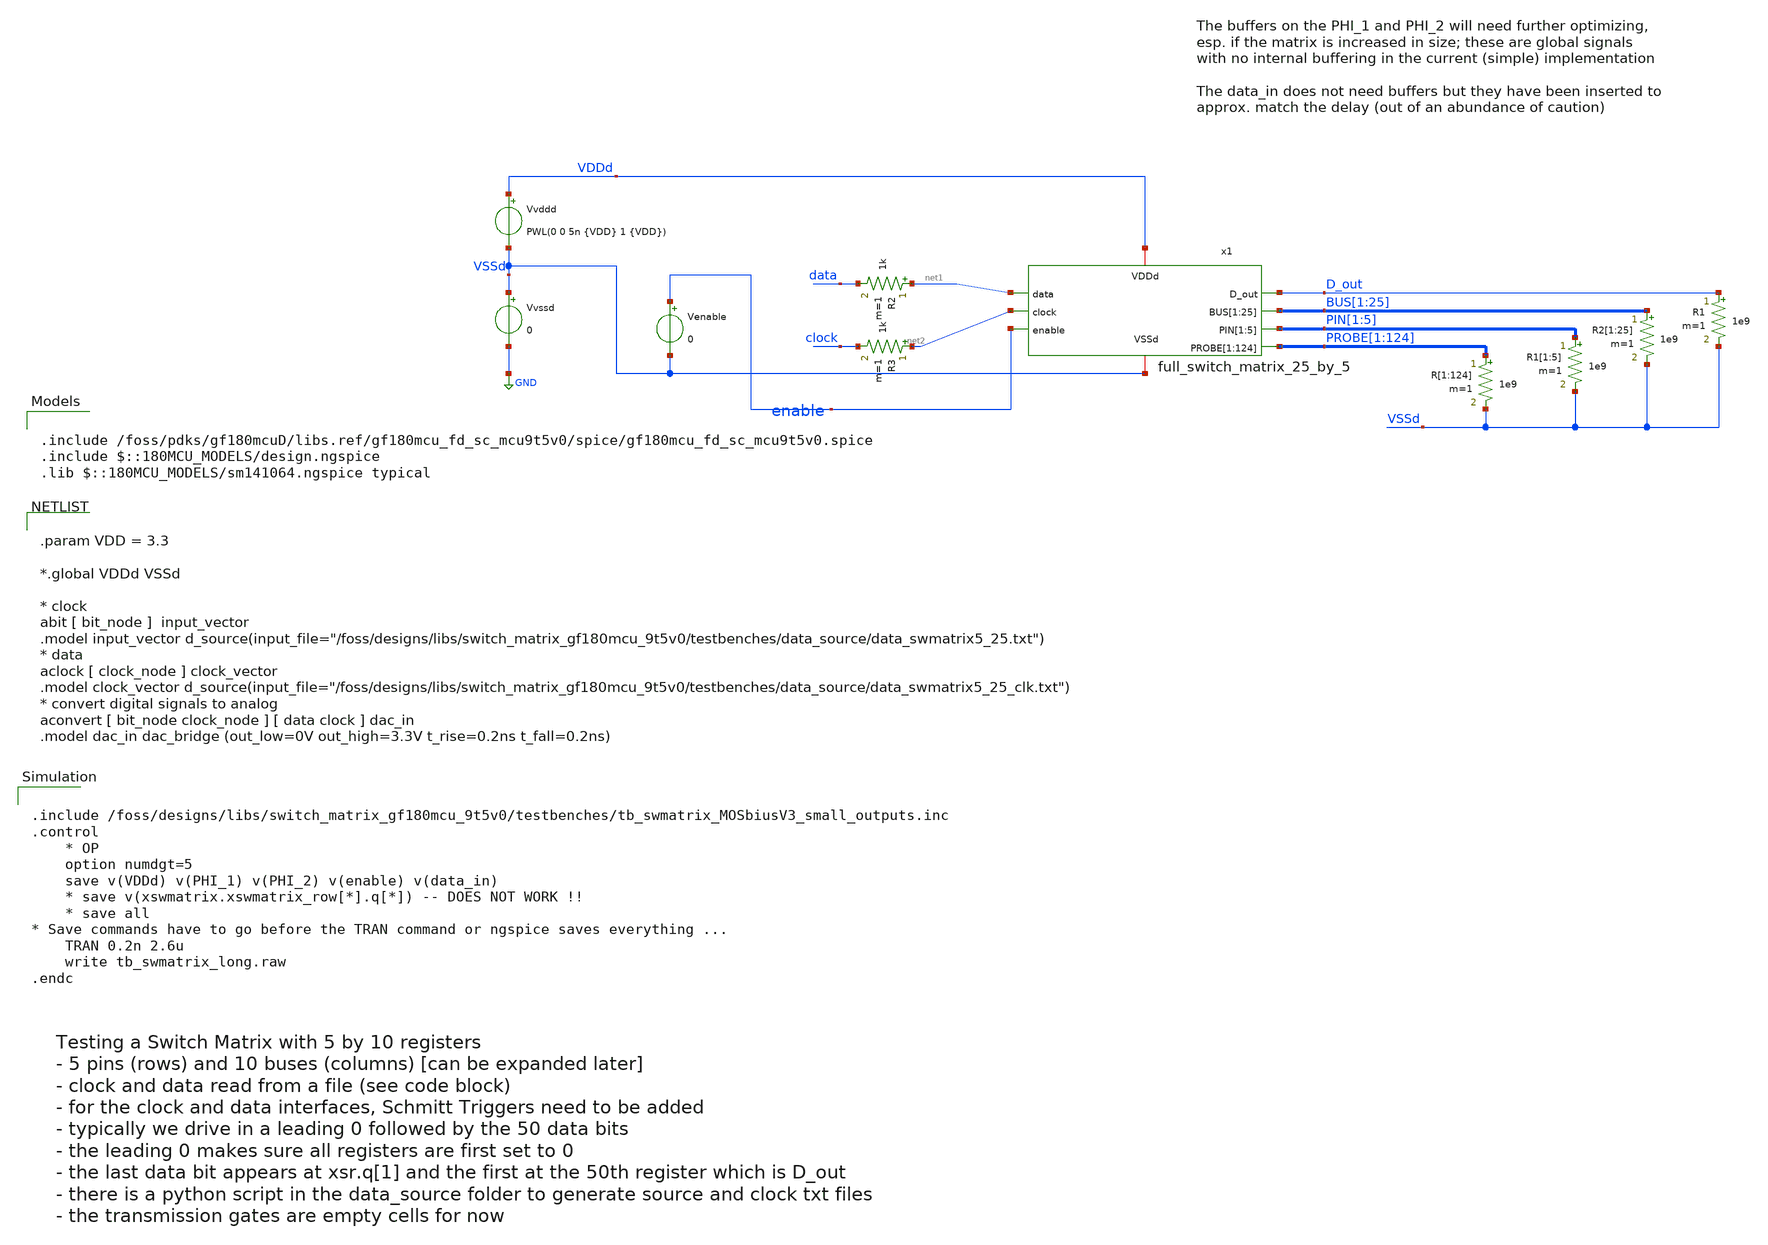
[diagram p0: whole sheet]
** sch_path: testbenches/tb_full_swmatrix_25_by_5.sch
**.subckt tb_full_swmatrix_25_by_5
Vvssd VSSd GND 0
Vvddd VDDd VSSd PWL(0 0 5n {VDD} 1 {VDD})
Venable enable VSSd 0
R2 net1 data 1k m=1
R3 net2 clock 1k m=1
x1 net1 D_out net2 BUS[1] BUS[2] BUS[3] BUS[4] BUS[5] BUS[6] BUS[7] BUS[8] BUS[9] BUS[10] BUS[11]
+ BUS[12] BUS[13] BUS[14] BUS[15] BUS[16] BUS[17] BUS[18] BUS[19] BUS[20] BUS[21] BUS[22] BUS[23] BUS[24]
+ BUS[25] PIN[1] PIN[2] PIN[3] PIN[4] PIN[5] enable VDDd VSSd PROBE[1] PROBE[2] PROBE[3] PROBE[4] PROBE[5]
+ PROBE[6] PROBE[7] PROBE[8] PROBE[9] PROBE[10] PROBE[11] PROBE[12] PROBE[13] PROBE[14] PROBE[15] PROBE[16]
+ PROBE[17] PROBE[18] PROBE[19] PROBE[20] PROBE[21] PROBE[22] PROBE[23] PROBE[24] PROBE[25] PROBE[26] PROBE[27]
+ PROBE[28] PROBE[29] PROBE[30] PROBE[31] PROBE[32] PROBE[33] PROBE[34] PROBE[35] PROBE[36] PROBE[37] PROBE[38]
+ PROBE[39] PROBE[40] PROBE[41] PROBE[42] PROBE[43] PROBE[44] PROBE[45] PROBE[46] PROBE[47] PROBE[48] PROBE[49]
+ PROBE[50] PROBE[51] PROBE[52] PROBE[53] PROBE[54] PROBE[55] PROBE[56] PROBE[57] PROBE[58] PROBE[59] PROBE[60]
+ PROBE[61] PROBE[62] PROBE[63] PROBE[64] PROBE[65] PROBE[66] PROBE[67] PROBE[68] PROBE[69] PROBE[70] PROBE[71]
+ PROBE[72] PROBE[73] PROBE[74] PROBE[75] PROBE[76] PROBE[77] PROBE[78] PROBE[79] PROBE[80] PROBE[81] PROBE[82]
+ PROBE[83] PROBE[84] PROBE[85] PROBE[86] PROBE[87] PROBE[88] PROBE[89] PROBE[90] PROBE[91] PROBE[92] PROBE[93]
+ PROBE[94] PROBE[95] PROBE[96] PROBE[97] PROBE[98] PROBE[99] PROBE[100] PROBE[101] PROBE[102] PROBE[103]
+ PROBE[104] PROBE[105] PROBE[106] PROBE[107] PROBE[108] PROBE[109] PROBE[110] PROBE[111] PROBE[112] PROBE[113]
+ PROBE[114] PROBE[115] PROBE[116] PROBE[117] PROBE[118] PROBE[119] PROBE[120] PROBE[121] PROBE[122] PROBE[123]
+ PROBE[124] full_switch_matrix_25_by_5
R[1] PROBE[1] VSSd 1e9 m=1
R[2] PROBE[2] VSSd 1e9 m=1
R[3] PROBE[3] VSSd 1e9 m=1
R[4] PROBE[4] VSSd 1e9 m=1
R[5] PROBE[5] VSSd 1e9 m=1
R[6] PROBE[6] VSSd 1e9 m=1
R[7] PROBE[7] VSSd 1e9 m=1
R[8] PROBE[8] VSSd 1e9 m=1
R[9] PROBE[9] VSSd 1e9 m=1
R[10] PROBE[10] VSSd 1e9 m=1
R[11] PROBE[11] VSSd 1e9 m=1
R[12] PROBE[12] VSSd 1e9 m=1
R[13] PROBE[13] VSSd 1e9 m=1
R[14] PROBE[14] VSSd 1e9 m=1
R[15] PROBE[15] VSSd 1e9 m=1
R[16] PROBE[16] VSSd 1e9 m=1
R[17] PROBE[17] VSSd 1e9 m=1
R[18] PROBE[18] VSSd 1e9 m=1
R[19] PROBE[19] VSSd 1e9 m=1
R[20] PROBE[20] VSSd 1e9 m=1
R[21] PROBE[21] VSSd 1e9 m=1
R[22] PROBE[22] VSSd 1e9 m=1
R[23] PROBE[23] VSSd 1e9 m=1
R[24] PROBE[24] VSSd 1e9 m=1
R[25] PROBE[25] VSSd 1e9 m=1
R[26] PROBE[26] VSSd 1e9 m=1
R[27] PROBE[27] VSSd 1e9 m=1
R[28] PROBE[28] VSSd 1e9 m=1
R[29] PROBE[29] VSSd 1e9 m=1
R[30] PROBE[30] VSSd 1e9 m=1
R[31] PROBE[31] VSSd 1e9 m=1
R[32] PROBE[32] VSSd 1e9 m=1
R[33] PROBE[33] VSSd 1e9 m=1
R[34] PROBE[34] VSSd 1e9 m=1
R[35] PROBE[35] VSSd 1e9 m=1
R[36] PROBE[36] VSSd 1e9 m=1
R[37] PROBE[37] VSSd 1e9 m=1
R[38] PROBE[38] VSSd 1e9 m=1
R[39] PROBE[39] VSSd 1e9 m=1
R[40] PROBE[40] VSSd 1e9 m=1
R[41] PROBE[41] VSSd 1e9 m=1
R[42] PROBE[42] VSSd 1e9 m=1
R[43] PROBE[43] VSSd 1e9 m=1
R[44] PROBE[44] VSSd 1e9 m=1
R[45] PROBE[45] VSSd 1e9 m=1
R[46] PROBE[46] VSSd 1e9 m=1
R[47] PROBE[47] VSSd 1e9 m=1
R[48] PROBE[48] VSSd 1e9 m=1
R[49] PROBE[49] VSSd 1e9 m=1
R[50] PROBE[50] VSSd 1e9 m=1
R[51] PROBE[51] VSSd 1e9 m=1
R[52] PROBE[52] VSSd 1e9 m=1
R[53] PROBE[53] VSSd 1e9 m=1
R[54] PROBE[54] VSSd 1e9 m=1
R[55] PROBE[55] VSSd 1e9 m=1
R[56] PROBE[56] VSSd 1e9 m=1
R[57] PROBE[57] VSSd 1e9 m=1
R[58] PROBE[58] VSSd 1e9 m=1
R[59] PROBE[59] VSSd 1e9 m=1
R[60] PROBE[60] VSSd 1e9 m=1
R[61] PROBE[61] VSSd 1e9 m=1
R[62] PROBE[62] VSSd 1e9 m=1
R[63] PROBE[63] VSSd 1e9 m=1
R[64] PROBE[64] VSSd 1e9 m=1
R[65] PROBE[65] VSSd 1e9 m=1
R[66] PROBE[66] VSSd 1e9 m=1
R[67] PROBE[67] VSSd 1e9 m=1
R[68] PROBE[68] VSSd 1e9 m=1
R[69] PROBE[69] VSSd 1e9 m=1
R[70] PROBE[70] VSSd 1e9 m=1
R[71] PROBE[71] VSSd 1e9 m=1
R[72] PROBE[72] VSSd 1e9 m=1
R[73] PROBE[73] VSSd 1e9 m=1
R[74] PROBE[74] VSSd 1e9 m=1
R[75] PROBE[75] VSSd 1e9 m=1
R[76] PROBE[76] VSSd 1e9 m=1
R[77] PROBE[77] VSSd 1e9 m=1
R[78] PROBE[78] VSSd 1e9 m=1
R[79] PROBE[79] VSSd 1e9 m=1
R[80] PROBE[80] VSSd 1e9 m=1
R[81] PROBE[81] VSSd 1e9 m=1
R[82] PROBE[82] VSSd 1e9 m=1
R[83] PROBE[83] VSSd 1e9 m=1
R[84] PROBE[84] VSSd 1e9 m=1
R[85] PROBE[85] VSSd 1e9 m=1
R[86] PROBE[86] VSSd 1e9 m=1
R[87] PROBE[87] VSSd 1e9 m=1
R[88] PROBE[88] VSSd 1e9 m=1
R[89] PROBE[89] VSSd 1e9 m=1
R[90] PROBE[90] VSSd 1e9 m=1
R[91] PROBE[91] VSSd 1e9 m=1
R[92] PROBE[92] VSSd 1e9 m=1
R[93] PROBE[93] VSSd 1e9 m=1
R[94] PROBE[94] VSSd 1e9 m=1
R[95] PROBE[95] VSSd 1e9 m=1
R[96] PROBE[96] VSSd 1e9 m=1
R[97] PROBE[97] VSSd 1e9 m=1
R[98] PROBE[98] VSSd 1e9 m=1
R[99] PROBE[99] VSSd 1e9 m=1
R[100] PROBE[100] VSSd 1e9 m=1
R[101] PROBE[101] VSSd 1e9 m=1
R[102] PROBE[102] VSSd 1e9 m=1
R[103] PROBE[103] VSSd 1e9 m=1
R[104] PROBE[104] VSSd 1e9 m=1
R[105] PROBE[105] VSSd 1e9 m=1
R[106] PROBE[106] VSSd 1e9 m=1
R[107] PROBE[107] VSSd 1e9 m=1
R[108] PROBE[108] VSSd 1e9 m=1
R[109] PROBE[109] VSSd 1e9 m=1
R[110] PROBE[110] VSSd 1e9 m=1
R[111] PROBE[111] VSSd 1e9 m=1
R[112] PROBE[112] VSSd 1e9 m=1
R[113] PROBE[113] VSSd 1e9 m=1
R[114] PROBE[114] VSSd 1e9 m=1
R[115] PROBE[115] VSSd 1e9 m=1
R[116] PROBE[116] VSSd 1e9 m=1
R[117] PROBE[117] VSSd 1e9 m=1
R[118] PROBE[118] VSSd 1e9 m=1
R[119] PROBE[119] VSSd 1e9 m=1
R[120] PROBE[120] VSSd 1e9 m=1
R[121] PROBE[121] VSSd 1e9 m=1
R[122] PROBE[122] VSSd 1e9 m=1
R[123] PROBE[123] VSSd 1e9 m=1
R[124] PROBE[124] VSSd 1e9 m=1
R1[1] PIN[1] VSSd 1e9 m=1
R1[2] PIN[2] VSSd 1e9 m=1
R1[3] PIN[3] VSSd 1e9 m=1
R1[4] PIN[4] VSSd 1e9 m=1
R1[5] PIN[5] VSSd 1e9 m=1
R2[1] BUS[1] VSSd 1e9 m=1
R2[2] BUS[2] VSSd 1e9 m=1
R2[3] BUS[3] VSSd 1e9 m=1
R2[4] BUS[4] VSSd 1e9 m=1
R2[5] BUS[5] VSSd 1e9 m=1
R2[6] BUS[6] VSSd 1e9 m=1
R2[7] BUS[7] VSSd 1e9 m=1
R2[8] BUS[8] VSSd 1e9 m=1
R2[9] BUS[9] VSSd 1e9 m=1
R2[10] BUS[10] VSSd 1e9 m=1
R2[11] BUS[11] VSSd 1e9 m=1
R2[12] BUS[12] VSSd 1e9 m=1
R2[13] BUS[13] VSSd 1e9 m=1
R2[14] BUS[14] VSSd 1e9 m=1
R2[15] BUS[15] VSSd 1e9 m=1
R2[16] BUS[16] VSSd 1e9 m=1
R2[17] BUS[17] VSSd 1e9 m=1
R2[18] BUS[18] VSSd 1e9 m=1
R2[19] BUS[19] VSSd 1e9 m=1
R2[20] BUS[20] VSSd 1e9 m=1
R2[21] BUS[21] VSSd 1e9 m=1
R2[22] BUS[22] VSSd 1e9 m=1
R2[23] BUS[23] VSSd 1e9 m=1
R2[24] BUS[24] VSSd 1e9 m=1
R2[25] BUS[25] VSSd 1e9 m=1
R1 D_out VSSd 1e9 m=1
**** begin user architecture code


.include /foss/designs/libs/switch_matrix_gf180mcu_9t5v0/testbenches/tb_swmatrix_MOSbiusV3_small_outputs.inc
.control
    * OP
    option numdgt=5
    save v(VDDd) v(PHI_1) v(PHI_2) v(enable) v(data_in)
    * save v(xswmatrix.xswmatrix_row[*].q[*]) -- DOES NOT WORK !!
    * save all
* Save commands have to go before the TRAN command or ngspice saves everything ...
    TRAN 0.2n 2.6u
    write tb_swmatrix_long.raw
.endc



.include /foss/pdks/gf180mcuD/libs.ref/gf180mcu_fd_sc_mcu9t5v0/spice/gf180mcu_fd_sc_mcu9t5v0.spice
.include $::180MCU_MODELS/design.ngspice
.lib $::180MCU_MODELS/sm141064.ngspice typical



.param VDD = 3.3

*.global VDDd VSSd

* clock
abit [ bit_node ]  input_vector
.model input_vector
+ d_source(input_file="/foss/designs/libs/switch_matrix_gf180mcu_9t5v0/testbenches/data_source/data_swmatrix5_25.txt")
* data
aclock [ clock_node ] clock_vector
.model clock_vector
+ d_source(input_file="/foss/designs/libs/switch_matrix_gf180mcu_9t5v0/testbenches/data_source/data_swmatrix5_25_clk.txt")
* convert digital signals to analog
aconvert [ bit_node clock_node ] [ data clock ] dac_in
.model dac_in dac_bridge (out_low=0V out_high=3.3V t_rise=0.2ns t_fall=0.2ns)


**** end user architecture code
**.ends
.GLOBAL GND
.end
